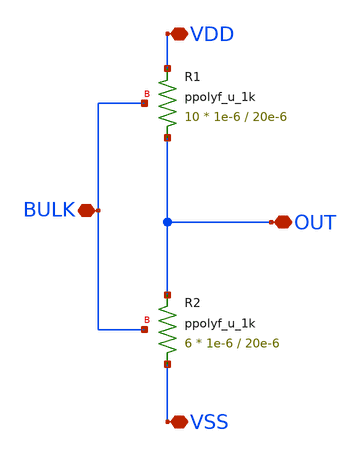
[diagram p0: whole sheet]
** sch_path: LDO/xschem/resistor/resistor.sch
**.subckt resistor OUT VSS VDD BULK
*.iopin OUT
*.iopin VSS
*.iopin VDD
*.iopin BULK
XR1 OUT VDD BULK ppolyf_u_1k r_width=1e-6 r_length=20e-6 m=10
XR2 VSS OUT BULK ppolyf_u_1k r_width=1e-6 r_length=20e-6 m=6
**.ends
.end
